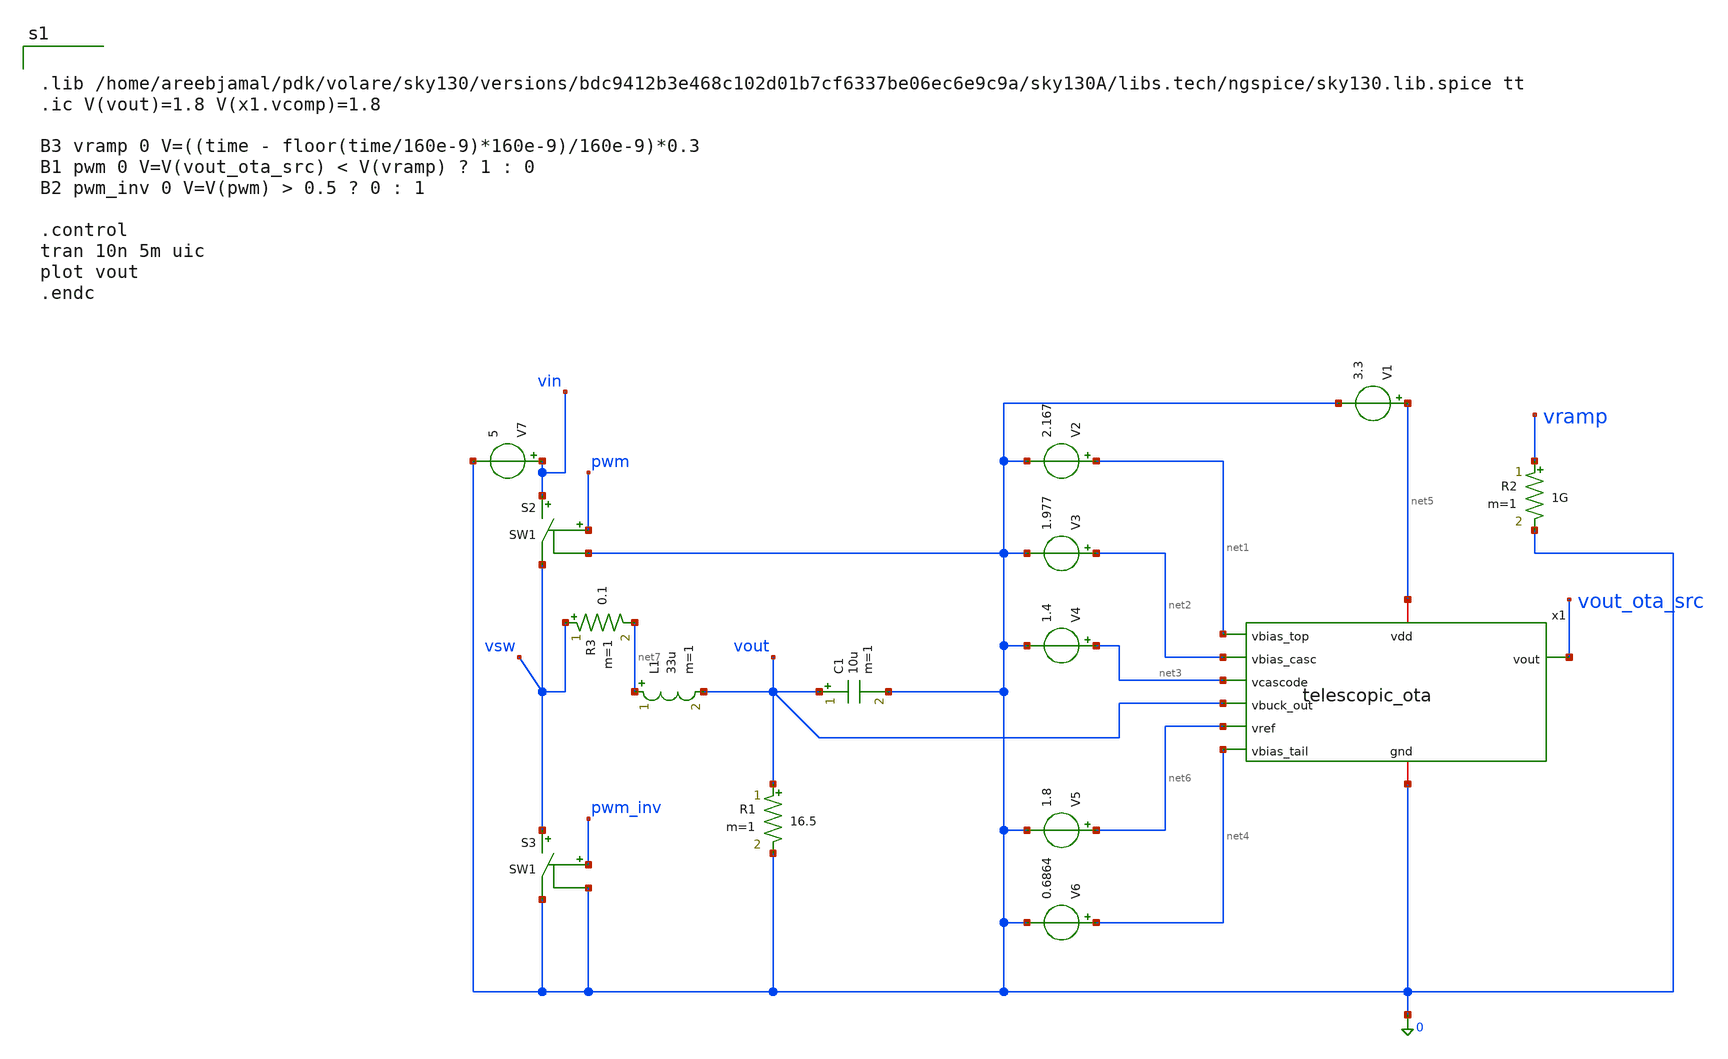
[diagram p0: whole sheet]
** sch_path: Buck_converter.sch
**.subckt Buck_converter
V1 net5 0 3.3
C1 vout 0 10u m=1
L1 net7 vout 33u m=1
R1 vout 0 16.5 m=1
x1 net5 net1 net2 vout_ota_src net3 vout net6 net4 0 telescopic_ota
V2 net1 0 2.167
V3 net2 0 1.977
V4 net3 0 1.4
V5 net6 0 1.8
V6 net4 0 0.6864
V7 vin 0 5
S2 vin vsw pwm 0 SW1
S3 vsw 0 pwm_inv 0 SW1
R2 vramp 0 1G m=1
R3 vsw net7 0.1 m=1
**** begin user architecture code


.lib /home/areebjamal/pdk/volare/sky130/versions/bdc9412b3e468c102d01b7cf6337be06ec6e9c9a/sky130A/libs.tech/ngspice/sky130.lib.spice tt
.ic V(vout)=1.8 V(x1.vcomp)=1.8

B3 vramp 0 V=((time - floor(time/160e-9)*160e-9)/160e-9)*0.3
B1 pwm 0 V=V(vout_ota_src) < V(vramp) ? 1 : 0
B2 pwm_inv 0 V=V(pwm) > 0.5 ? 0 : 1

.control
tran 10n 5m uic
plot vout
.endc


**** end user architecture code
**.ends

* expanding   symbol:  telescopic_ota.sym # of pins=9
** sym_path: telescopic_ota.sym
** sch_path: telescopic_ota.sch
.subckt telescopic_ota vdd vbias_top vbias_casc vout vcascode vbuck_out vref vbias_tail gnd
*.ipin vbias_top
*.ipin vbias_casc
*.ipin vcascode
*.ipin vbuck_out
*.ipin vref
*.ipin vbias_tail
*.opin vout
*.iopin vdd
*.iopin gnd
XM3 net3 vcascode vy gnd sky130_fd_pr__nfet_01v8 L=1 W=5.6 nf=1 ad='int((1 + 1)/2) * 5.6 / 1 * 0.29'
+ as='int((1 + 2)/2) * 5.6 / 1 * 0.29' pd='2*int((1 + 1)/2) * (5.6 / 1 + 0.29)' ps='2*int((1 + 2)/2) * (5.6 / 1 + 0.29)'
+ nrd='0.29 / 5.6 ' nrs='0.29 / 5.6 ' sa=0 sb=0 sd=0 mult=1 m=1
XM8 net2 vbias_top vdd vdd sky130_fd_pr__pfet_01v8 L=1 W=16.8 nf=1 ad='int((1 + 1)/2) * 16.8 / 1 * 0.29'
+ as='int((1 + 2)/2) * 16.8 / 1 * 0.29' pd='2*int((1 + 1)/2) * (16.8 / 1 + 0.29)' ps='2*int((1 + 2)/2) * (16.8 / 1 + 0.29)'
+ nrd='0.29 / 16.8 ' nrs='0.29 / 16.8 ' sa=0 sb=0 sd=0 mult=1 m=1
XM7 net1 vbias_top vdd vdd sky130_fd_pr__pfet_01v8 L=1 W=16.8 nf=1 ad='int((1 + 1)/2) * 16.8 / 1 * 0.29'
+ as='int((1 + 2)/2) * 16.8 / 1 * 0.29' pd='2*int((1 + 1)/2) * (16.8 / 1 + 0.29)' ps='2*int((1 + 2)/2) * (16.8 / 1 + 0.29)'
+ nrd='0.29 / 16.8 ' nrs='0.29 / 16.8 ' sa=0 sb=0 sd=0 mult=1 m=1
XM5 net3 vbias_casc net1 vdd sky130_fd_pr__pfet_01v8 L=1 W=16.8 nf=1 ad='int((1 + 1)/2) * 16.8 / 1 * 0.29'
+ as='int((1 + 2)/2) * 16.8 / 1 * 0.29' pd='2*int((1 + 1)/2) * (16.8 / 1 + 0.29)' ps='2*int((1 + 2)/2) * (16.8 / 1 + 0.29)'
+ nrd='0.29 / 16.8 ' nrs='0.29 / 16.8 ' sa=0 sb=0 sd=0 mult=1 m=1
XM6 vout vbias_casc net2 vdd sky130_fd_pr__pfet_01v8 L=1 W=16.8 nf=1 ad='int((1 + 1)/2) * 16.8 / 1 * 0.29'
+ as='int((1 + 2)/2) * 16.8 / 1 * 0.29' pd='2*int((1 + 1)/2) * (16.8 / 1 + 0.29)' ps='2*int((1 + 2)/2) * (16.8 / 1 + 0.29)'
+ nrd='0.29 / 16.8 ' nrs='0.29 / 16.8 ' sa=0 sb=0 sd=0 mult=1 m=1
XM1 vy vbuck_out net5 gnd sky130_fd_pr__nfet_01v8 L=1 W=5.6 nf=1 ad='int((1 + 1)/2) * 5.6 / 1 * 0.29'
+ as='int((1 + 2)/2) * 5.6 / 1 * 0.29' pd='2*int((1 + 1)/2) * (5.6 / 1 + 0.29)' ps='2*int((1 + 2)/2) * (5.6 / 1 + 0.29)'
+ nrd='0.29 / 5.6 ' nrs='0.29 / 5.6 ' sa=0 sb=0 sd=0 mult=1 m=1
XM4 vout vcascode net4 gnd sky130_fd_pr__nfet_01v8 L=1 W=5.6 nf=1 ad='int((1 + 1)/2) * 5.6 / 1 * 0.29'
+ as='int((1 + 2)/2) * 5.6 / 1 * 0.29' pd='2*int((1 + 1)/2) * (5.6 / 1 + 0.29)' ps='2*int((1 + 2)/2) * (5.6 / 1 + 0.29)'
+ nrd='0.29 / 5.6 ' nrs='0.29 / 5.6 ' sa=0 sb=0 sd=0 mult=1 m=1
XM2 net4 vref net5 gnd sky130_fd_pr__nfet_01v8 L=1 W=5.6 nf=1 ad='int((1 + 1)/2) * 5.6 / 1 * 0.29' as='int((1 + 2)/2) * 5.6 / 1 * 0.29'
+ pd='2*int((1 + 1)/2) * (5.6 / 1 + 0.29)' ps='2*int((1 + 2)/2) * (5.6 / 1 + 0.29)' nrd='0.29 / 5.6 ' nrs='0.29 / 5.6 '
+ sa=0 sb=0 sd=0 mult=1 m=1
XM9 net5 vbias_tail gnd gnd sky130_fd_pr__nfet_01v8 L=1 W=11.2 nf=1 ad='int((1 + 1)/2) * 11.2 / 1 * 0.29'
+ as='int((1 + 2)/2) * 11.2 / 1 * 0.29' pd='2*int((1 + 1)/2) * (11.2 / 1 + 0.29)' ps='2*int((1 + 2)/2) * (11.2 / 1 + 0.29)'
+ nrd='0.29 / 11.2 ' nrs='0.29 / 11.2 ' sa=0 sb=0 sd=0 mult=1 m=1
R1 vout vcomp 360k m=1
C1 vcomp gnd 100p m=1
.ends

**** begin user architecture code
.MODEL SW1 SW  VT=0.5 VH=0.1  RON=0.01 ROFF=1e9
**** end user architecture code
.end
